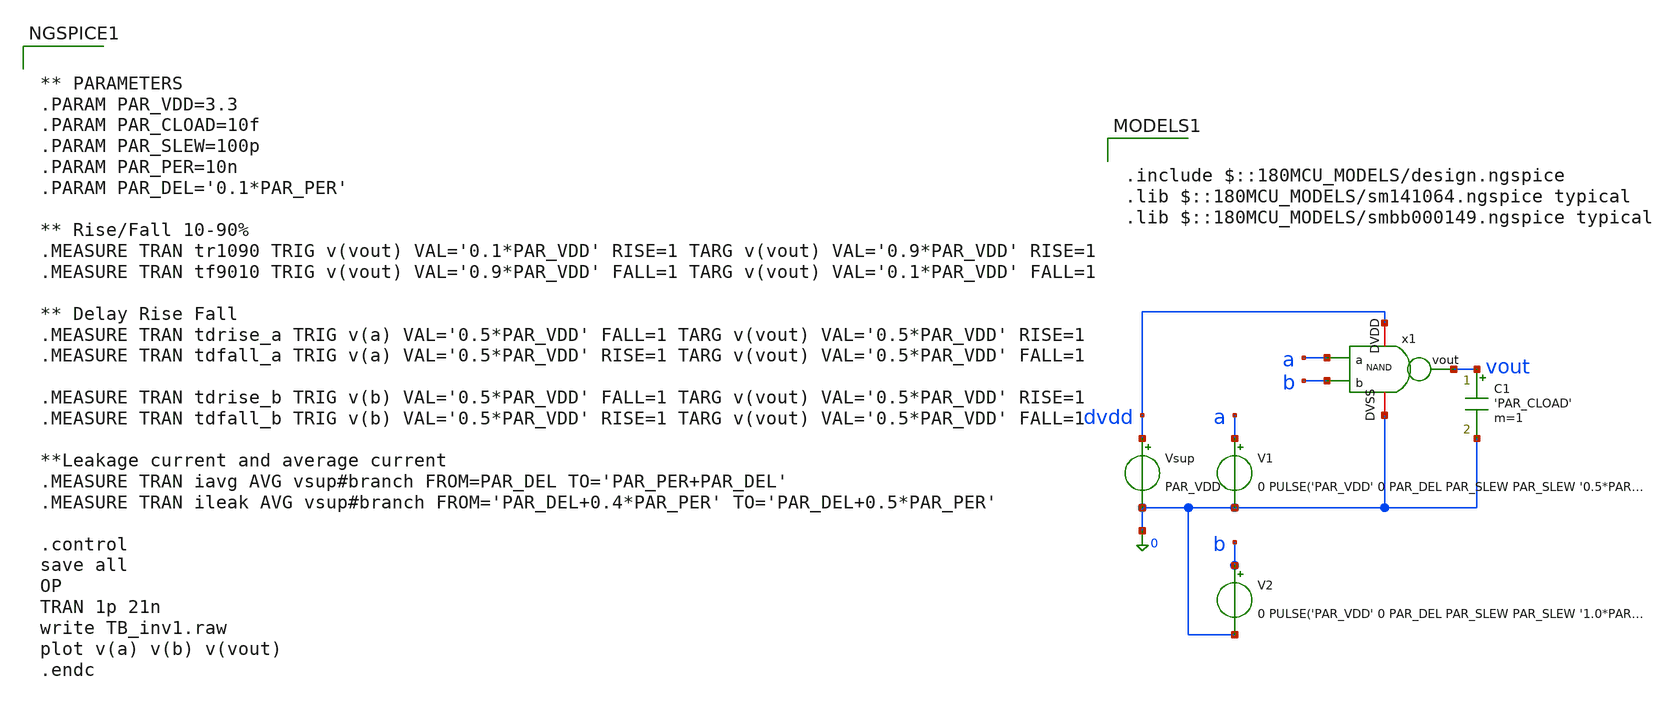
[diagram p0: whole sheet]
** sch_path: src/schematic/DFF/TB_NAND.sch
**.subckt TB_NAND
V1 a 0 0 PULSE('PAR_VDD' 0 PAR_DEL PAR_SLEW PAR_SLEW '0.5*PAR_PER' '1.0*PAR_PER')
Vsup dvdd 0 PAR_VDD
C1 vout 0 'PAR_CLOAD' m=1
x1 dvdd vout a b 0 NAND
V2 b 0 0 PULSE('PAR_VDD' 0 PAR_DEL PAR_SLEW PAR_SLEW '1.0*PAR_PER' '2.0*PAR_PER')
**** begin user architecture code

.include $::180MCU_MODELS/design.ngspice
.lib $::180MCU_MODELS/sm141064.ngspice typical
.lib $::180MCU_MODELS/smbb000149.ngspice typical



** PARAMETERS
.PARAM PAR_VDD=3.3
.PARAM PAR_CLOAD=10f
.PARAM PAR_SLEW=100p
.PARAM PAR_PER=10n
.PARAM PAR_DEL='0.1*PAR_PER'

** Rise/Fall 10-90%
.MEASURE TRAN tr1090 TRIG v(vout) VAL='0.1*PAR_VDD' RISE=1 TARG v(vout) VAL='0.9*PAR_VDD' RISE=1
.MEASURE TRAN tf9010 TRIG v(vout) VAL='0.9*PAR_VDD' FALL=1 TARG v(vout) VAL='0.1*PAR_VDD' FALL=1

** Delay Rise Fall
.MEASURE TRAN tdrise_a TRIG v(a) VAL='0.5*PAR_VDD' FALL=1 TARG v(vout) VAL='0.5*PAR_VDD' RISE=1
.MEASURE TRAN tdfall_a TRIG v(a) VAL='0.5*PAR_VDD' RISE=1 TARG v(vout) VAL='0.5*PAR_VDD' FALL=1

.MEASURE TRAN tdrise_b TRIG v(b) VAL='0.5*PAR_VDD' FALL=1 TARG v(vout) VAL='0.5*PAR_VDD' RISE=1
.MEASURE TRAN tdfall_b TRIG v(b) VAL='0.5*PAR_VDD' RISE=1 TARG v(vout) VAL='0.5*PAR_VDD' FALL=1

**Leakage current and average current
.MEASURE TRAN iavg AVG vsup#branch FROM=PAR_DEL TO='PAR_PER+PAR_DEL'
.MEASURE TRAN ileak AVG vsup#branch FROM='PAR_DEL+0.4*PAR_PER' TO='PAR_DEL+0.5*PAR_PER'

.control
save all
OP
TRAN 1p 21n
write TB_inv1.raw
plot v(a) v(b) v(vout)
.endc


**** end user architecture code
**.ends

* expanding   symbol:  Chipaton2026/src/schematic/DFF/NAND.sym # of pins=5
** sym_path: src/schematic/NAND/NAND.sym
** sch_path: src/schematic/NAND/NAND.sch
.subckt NAND DVDD vout a b DVSS
*.ipin a
*.opin vout
*.iopin DVDD
*.iopin DVSS
*.ipin b
XM3 vout a DVDD DVDD pfet_03v3 L=0.3u W=1.7u nf=1 ad='int((nf+1)/2) * W/nf * 0.18u' as='int((nf+2)/2) * W/nf * 0.18u'
+ pd='2*int((nf+1)/2) * (W/nf + 0.18u)' ps='2*int((nf+2)/2) * (W/nf + 0.18u)' nrd='0.18u / W' nrs='0.18u / W'
+ sa=0 sb=0 sd=0 m=1
XM4 vout a net1 DVSS nfet_03v3 L=0.3u W=0.85u nf=1 ad='int((nf+1)/2) * W/nf * 0.18u' as='int((nf+2)/2) * W/nf * 0.18u'
+ pd='2*int((nf+1)/2) * (W/nf + 0.18u)' ps='2*int((nf+2)/2) * (W/nf + 0.18u)' nrd='0.18u / W' nrs='0.18u / W'
+ sa=0 sb=0 sd=0 m=1
XM1 vout b DVDD DVDD pfet_03v3 L=0.3u W=1.7u nf=1 ad='int((nf+1)/2) * W/nf * 0.18u' as='int((nf+2)/2) * W/nf * 0.18u'
+ pd='2*int((nf+1)/2) * (W/nf + 0.18u)' ps='2*int((nf+2)/2) * (W/nf + 0.18u)' nrd='0.18u / W' nrs='0.18u / W'
+ sa=0 sb=0 sd=0 m=1
XM2 net1 b DVSS DVSS nfet_03v3 L=0.3u W=0.85u nf=1 ad='int((nf+1)/2) * W/nf * 0.18u' as='int((nf+2)/2) * W/nf * 0.18u'
+ pd='2*int((nf+1)/2) * (W/nf + 0.18u)' ps='2*int((nf+2)/2) * (W/nf + 0.18u)' nrd='0.18u / W' nrs='0.18u / W'
+ sa=0 sb=0 sd=0 m=1
.ends

.end
